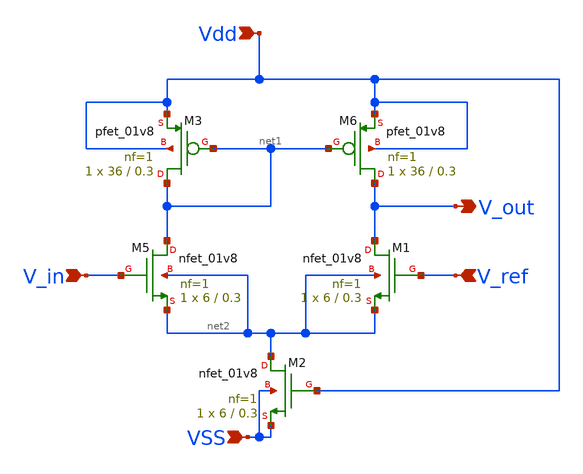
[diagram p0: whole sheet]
** sch_path: schematics_xschem/OpAmp_Comparator.sch
**.subckt OpAmp_Comparator V_out V_in V_ref Vdd VSS
*.opin V_out
*.ipin V_in
*.ipin V_ref
*.ipin Vdd
*.ipin VSS
XM5 net1 V_in net2 net2 sky130_fd_pr__nfet_01v8 L=0.3 W=6 nf=1 ad='int((nf+1)/2) * W/nf * 0.29' as='int((nf+2)/2) * W/nf * 0.29'
+ pd='2*int((nf+1)/2) * (W/nf + 0.29)' ps='2*int((nf+2)/2) * (W/nf + 0.29)' nrd='0.29 / W' nrs='0.29 / W'
+ sa=0 sb=0 sd=0 mult=1 m=1
XM6 V_out net1 Vdd Vdd sky130_fd_pr__pfet_01v8 L=0.3 W=36 nf=1 ad='int((nf+1)/2) * W/nf * 0.29' as='int((nf+2)/2) * W/nf * 0.29'
+ pd='2*int((nf+1)/2) * (W/nf + 0.29)' ps='2*int((nf+2)/2) * (W/nf + 0.29)' nrd='0.29 / W' nrs='0.29 / W'
+ sa=0 sb=0 sd=0 mult=1 m=1
XM3 net1 net1 Vdd Vdd sky130_fd_pr__pfet_01v8 L=0.3 W=36 nf=1 ad='int((nf+1)/2) * W/nf * 0.29' as='int((nf+2)/2) * W/nf * 0.29'
+ pd='2*int((nf+1)/2) * (W/nf + 0.29)' ps='2*int((nf+2)/2) * (W/nf + 0.29)' nrd='0.29 / W' nrs='0.29 / W'
+ sa=0 sb=0 sd=0 mult=1 m=1
XM1 V_out V_ref net2 net2 sky130_fd_pr__nfet_01v8 L=0.3 W=6 nf=1 ad='int((nf+1)/2) * W/nf * 0.29' as='int((nf+2)/2) * W/nf * 0.29'
+ pd='2*int((nf+1)/2) * (W/nf + 0.29)' ps='2*int((nf+2)/2) * (W/nf + 0.29)' nrd='0.29 / W' nrs='0.29 / W'
+ sa=0 sb=0 sd=0 mult=1 m=1
XM2 net2 Vdd VSS VSS sky130_fd_pr__nfet_01v8 L=0.3 W=6 nf=1 ad='int((nf+1)/2) * W/nf * 0.29' as='int((nf+2)/2) * W/nf * 0.29'
+ pd='2*int((nf+1)/2) * (W/nf + 0.29)' ps='2*int((nf+2)/2) * (W/nf + 0.29)' nrd='0.29 / W' nrs='0.29 / W'
+ sa=0 sb=0 sd=0 mult=1 m=1
**.ends
.end
